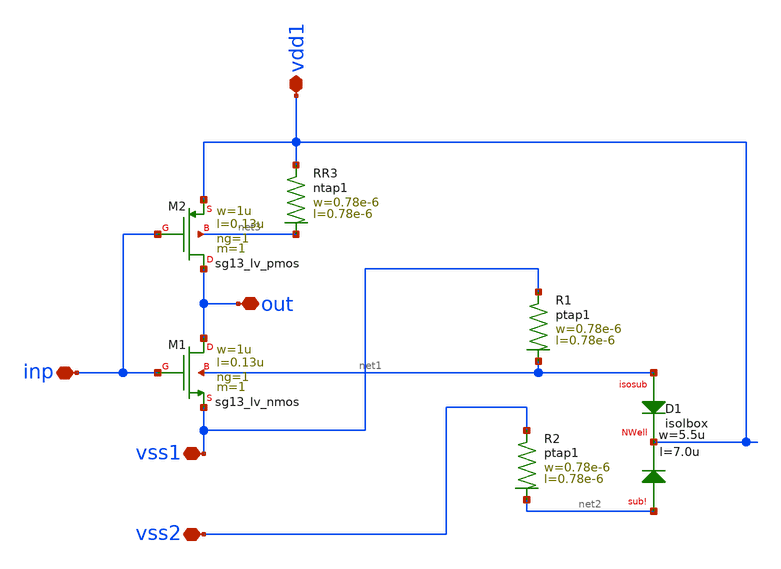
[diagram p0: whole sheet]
** sch_path: deepNWell/schematic/nmos_iso_ref.sch
**.subckt nmos_iso_ref inp out vss1 vdd1 vss2
*.iopin inp
*.iopin out
*.iopin vss1
*.iopin vdd1
*.iopin vss2
XM1 out inp vss1 net1 sg13_lv_nmos w=1u l=0.13u ng=1 m=1 mm_ok=1
XD1 net1 vdd1 net2 isolbox l=7.0u w=5.5u
XR1 vss1 net1 ptap1 R=262.8 w=0.78e-6 l=0.78e-6
XR2 vss2 net2 ptap1 R=262.8 w=0.78e-6 l=0.78e-6
XM2 out inp vdd1 net3 sg13_lv_pmos w=1u l=0.13u ng=1 m=1 mm_ok=1
XR3 vdd1 net3 ntap1 R=262.8 w=0.78e-6 l=0.78e-6
**.ends
.end
